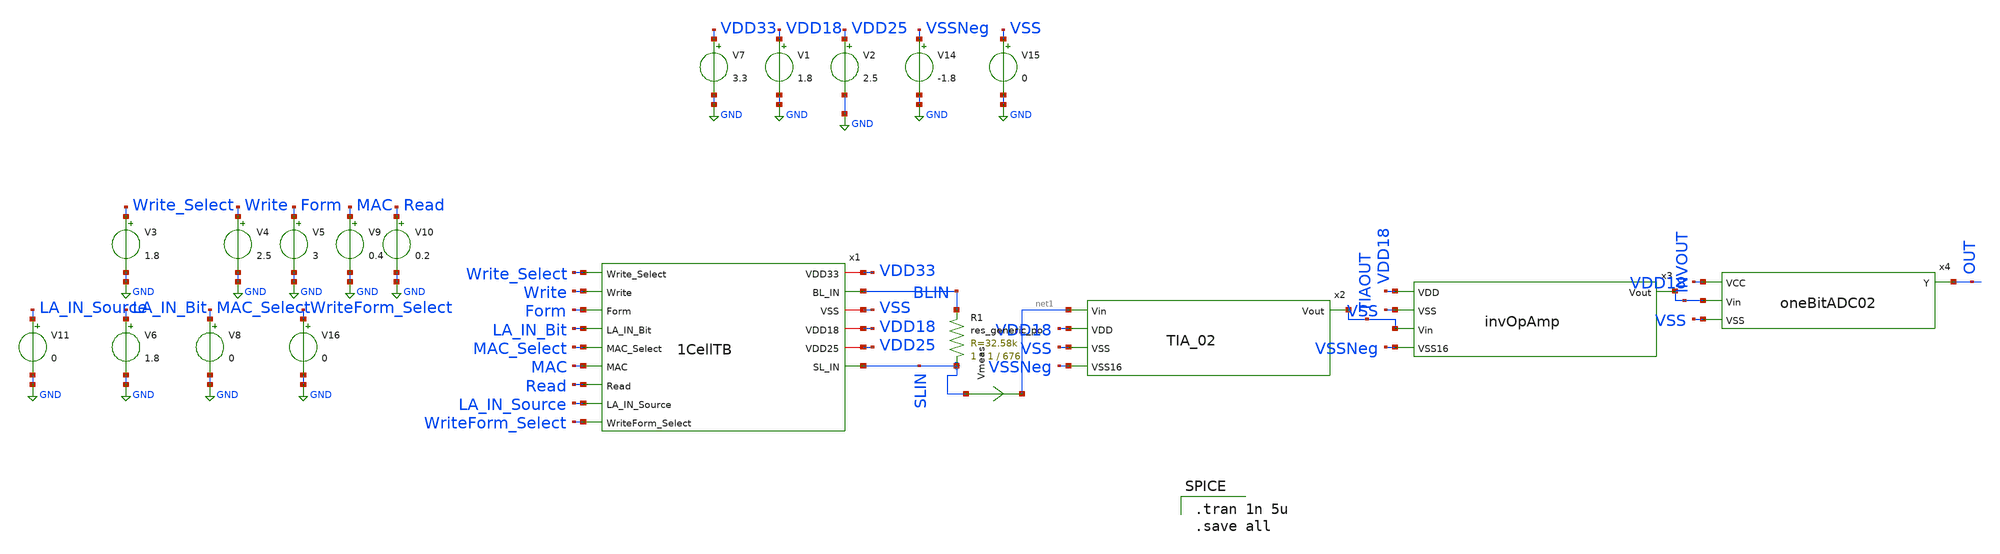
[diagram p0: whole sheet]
** sch_path: 1Cell__TB02.sch
**.subckt 1Cell__TB02
x1 VDD33 Write_Select Write Form LA_IN_Bit MAC_Select BLIN MAC Read VSS VDD18 VDD25 LA_IN_Source
+ SLIN WriteForm_Select 1CellTB
V7 VDD33 GND 3.3
V1 VDD18 GND 1.8
V2 VDD25 GND 2.5
V3 Write_Select GND 1.8
V4 Write GND 2.5
V5 Form GND 3
V6 LA_IN_Bit GND 1.8
V8 MAC_Select GND 0
V9 MAC GND 0.4
V10 Read GND 0.2
V11 LA_IN_Source GND 0
x2 net1 VDD18 TIAOUT VSS VSSNeg TIA_02
x3 INVOUT VDD18 VSS TIAOUT VSSNeg invOpAmp
V14 VSSNeg GND -1.8
XR1 SLIN BLIN sky130_fd_pr__res_generic_po W=1 L=676 m=1
V15 VSS GND 0
Vmeas SLIN net1 0
.save i(vmeas)
V16 WriteForm_Select GND 0
x4 VDD18 OUT INVOUT VSS oneBitADC02
**** begin user architecture code
.lib $::SKYWATER_MODELS/sky130.lib.spice ss

.tran 1n 5u
.save all

**** end user architecture code
**.ends
.GLOBAL GND
.end
